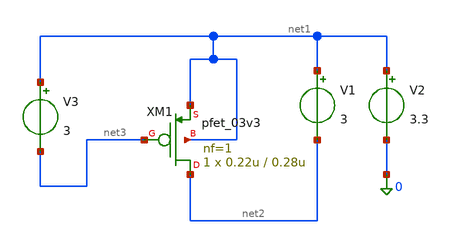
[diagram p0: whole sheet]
** sch_path: karakterisasi_p3v3.sch
**.subckt karakterisasi_p3v3
XM1 net2 net3 net1 net1 pfet_03v3 L=0.28u W=0.22u nf=1 ad='int((nf+1)/2) * W/nf * 0.18u' as='int((nf+2)/2) * W/nf * 0.18u'
+ pd='2*int((nf+1)/2) * (W/nf + 0.18u)' ps='2*int((nf+2)/2) * (W/nf + 0.18u)' nrd='0.18u / W' nrs='0.18u / W'
+ sa=0 sb=0 sd=0 m=1
V1 net1 net2 3
V2 net1 0 3.3
V3 net1 net3 3
**.ends
.end
